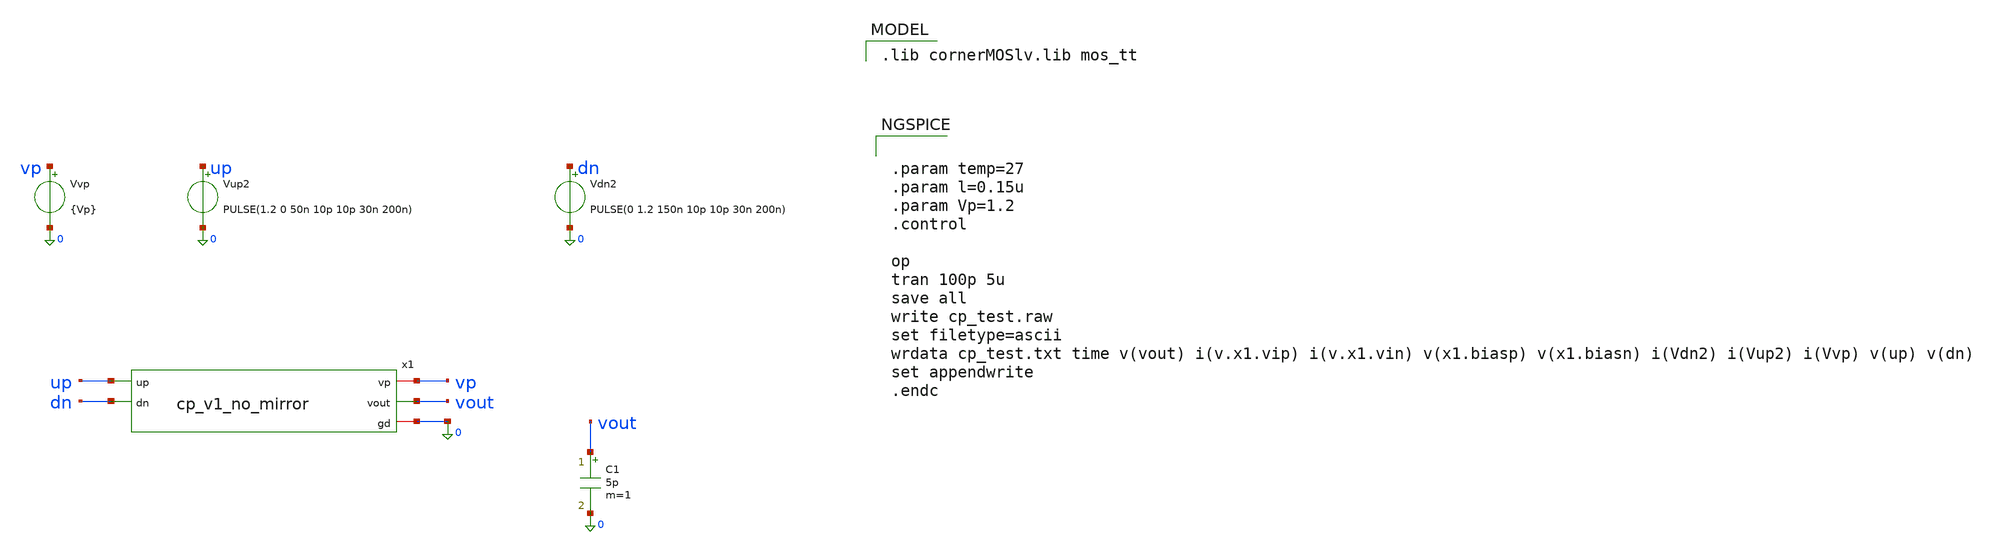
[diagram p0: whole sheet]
** sch_path: PLL0663-main/schematic/xschem/charge_pump/old_sch/cp_v1_tb_tran.sch
**.subckt cp_v1_tb_tran
Vvp vp 0 {Vp}
C1 vout 0 5p m=1
Vup2 up 0 PULSE(1.2 0 50n 10p 10p 30n 200n)
Vdn2 dn 0 PULSE(0 1.2 150n 10p 10p 30n 200n)
x1 vp up vout dn 0 cp_v1_no_mirror
**** begin user architecture code
 .lib cornerMOSlv.lib mos_tt



.param temp=27
.param l=0.15u
.param Vp=1.2
.control

op
tran 100p 5u
save all
write cp_test.raw
set filetype=ascii
wrdata cp_test.txt time v(vout) i(v.x1.vip) i(v.x1.vin) v(x1.biasp) v(x1.biasn) i(Vdn2) i(Vup2)
+ i(Vvp) v(up) v(dn)
set appendwrite
.endc


**** end user architecture code
**.ends
.end
